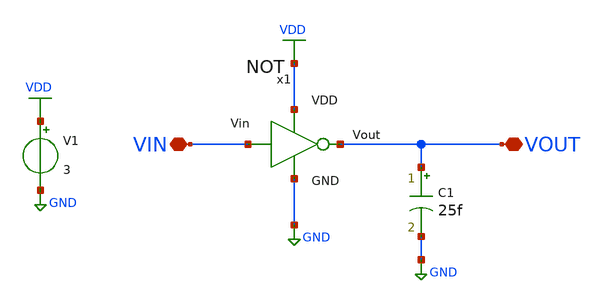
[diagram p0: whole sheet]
** sch_path: Taller2_extendido/Insumos/NOT_TEST.sch
**.subckt NOT_TEST VOUT VIN
*.iopin VOUT
*.iopin VIN
x1 VDD VIN VOUT GND NOT
C1 VOUT GND 25f m=1
V1 VDD GND 3
**** begin user architecture code


.lib cornerMOShv.lib mos_tt
.lib cornerMOSlv.lib mos_tt
*.lib cornerMOShv.lib mos_ff
*.lib cornerMOSlv.lib mos_ff
*.lib cornerMOShv.lib mos_ss
*.lib cornerMOSlv.lib mos_ss
*.lib cornerMOShv.lib mos_sf
*.lib cornerMOSlv.lib mos_sf
*.lib cornerMOShv.lib mos_fs
*.lib cornerMOSlv.lib mos_fs

*.include /opt/pdks/ihp-sg13g2/libs.ref/sg13g2_stdcell/spice/sg13g2_stdcell.spice
*.lib $::SG13G2_MODELS/cornerRES.lib res_typ
*.lib $::SG13G2_MODELS/cornerCAP.lib cap_typ
*.lib $::SG13G2_MODELS/diodes.lib



vin VIN 0 PULSE(0 3.3 1ns 0ns 0ns 2ns 4ns)
.control
save all
***********************************************
* Ingresar comando de simulación transiente acá



* *********************************************
plot V(VIN) v(VOUT)
meas tran tpHL_in FIND time WHEN v(VIN)=0.9 TD=0 FALL=1
meas tran tpHL_fin FIND time WHEN v(VOUT)=0.9 TD=0 RISE=1
print tpHL_fin - tpHL_in
.endc


**** end user architecture code
**.ends

* expanding   symbol:  NOT.sym # of pins=4
** sym_path: Taller2/Insumos/NOT.sym
** sch_path: Taller2/Insumos/NOT.sch
.subckt NOT VDD Vin Vout GND
*.ipin VDD
*.ipin Vin
*.ipin GND
*.opin Vout
XM3 GND Vin Vout GND sg13_hv_nmos w=1.0u l=0.45u ng=1 m=1 mm_ok=1
XM4 Vout Vin VDD VDD sg13_hv_pmos w=2.72u l=0.45u ng=1 m=1 mm_ok=1
.ends

.GLOBAL VDD
.GLOBAL GND
.end
